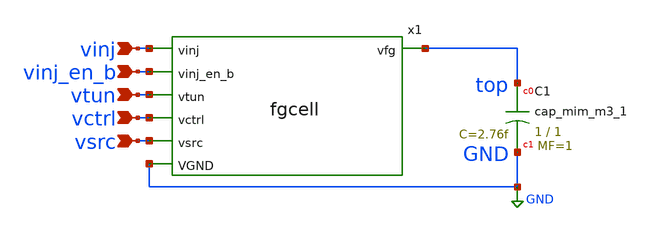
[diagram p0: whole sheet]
** sch_path: FG_MiM_cap/FG_MiM_cap.sch
**.subckt FG_MiM_cap vinj vinj_en_b vtun vctrl vsrc
*.ipin vinj
*.ipin vinj_en_b
*.ipin vtun
*.ipin vctrl
*.ipin vsrc
x1 vinj vinj_en_b vtun vctrl vsrc GND top fgcell
XC1 top GND sky130_fd_pr__cap_mim_m3_1 W=1 L=1 MF=1 m=1
**.ends

* expanding   symbol:
*+  /Users/dalejulson/Desktop/OpenCircuitDesign/ci2406_fgcaptest/xschem/fgcell.sym # of pins=7
** sym_path: xschem/fgcell.sym
** sch_path: xschem/fgcell.sch
.subckt fgcell vinj vinj_en_b vtun vctrl vsrc VGND vfg
*.ipin vinj
*.ipin vinj_en_b
*.ipin vtun
*.ipin vctrl
*.ipin vsrc
*.ipin VGND
*.opin vfg
XM1 vsrc vfg net1 vinj sky130_fd_pr__pfet_g5v0d10v5 L=0.5 W=1 nf=1 ad='int((nf+1)/2) * W/nf * 0.29' as='int((nf+2)/2) * W/nf * 0.29'
+ pd='2*int((nf+1)/2) * (W/nf + 0.29)' ps='2*int((nf+2)/2) * (W/nf + 0.29)' nrd='0.29 / W' nrs='0.29 / W'
+ sa=0 sb=0 sd=0 mult=1 m=1
XM2 net1 vinj_en_b vinj vinj sky130_fd_pr__pfet_g5v0d10v5 L=0.5 W=1 nf=1 ad='int((nf+1)/2) * W/nf * 0.29'
+ as='int((nf+2)/2) * W/nf * 0.29' pd='2*int((nf+1)/2) * (W/nf + 0.29)' ps='2*int((nf+2)/2) * (W/nf + 0.29)'
+ nrd='0.29 / W' nrs='0.29 / W' sa=0 sb=0 sd=0 mult=1 m=1
XC1 vfg vtun VGND sky130_fd_pr__cap_var_hvt W=1 L=0.5 VM=1 m=1
XM3 vctrl vfg vctrl vctrl sky130_fd_pr__pfet_g5v0d10v5 L=0.5 W=1 nf=1 ad='int((nf+1)/2) * W/nf * 0.29'
+ as='int((nf+2)/2) * W/nf * 0.29' pd='2*int((nf+1)/2) * (W/nf + 0.29)' ps='2*int((nf+2)/2) * (W/nf + 0.29)'
+ nrd='0.29 / W' nrs='0.29 / W' sa=0 sb=0 sd=0 mult=1 m=1
.ends

.GLOBAL GND
.end
